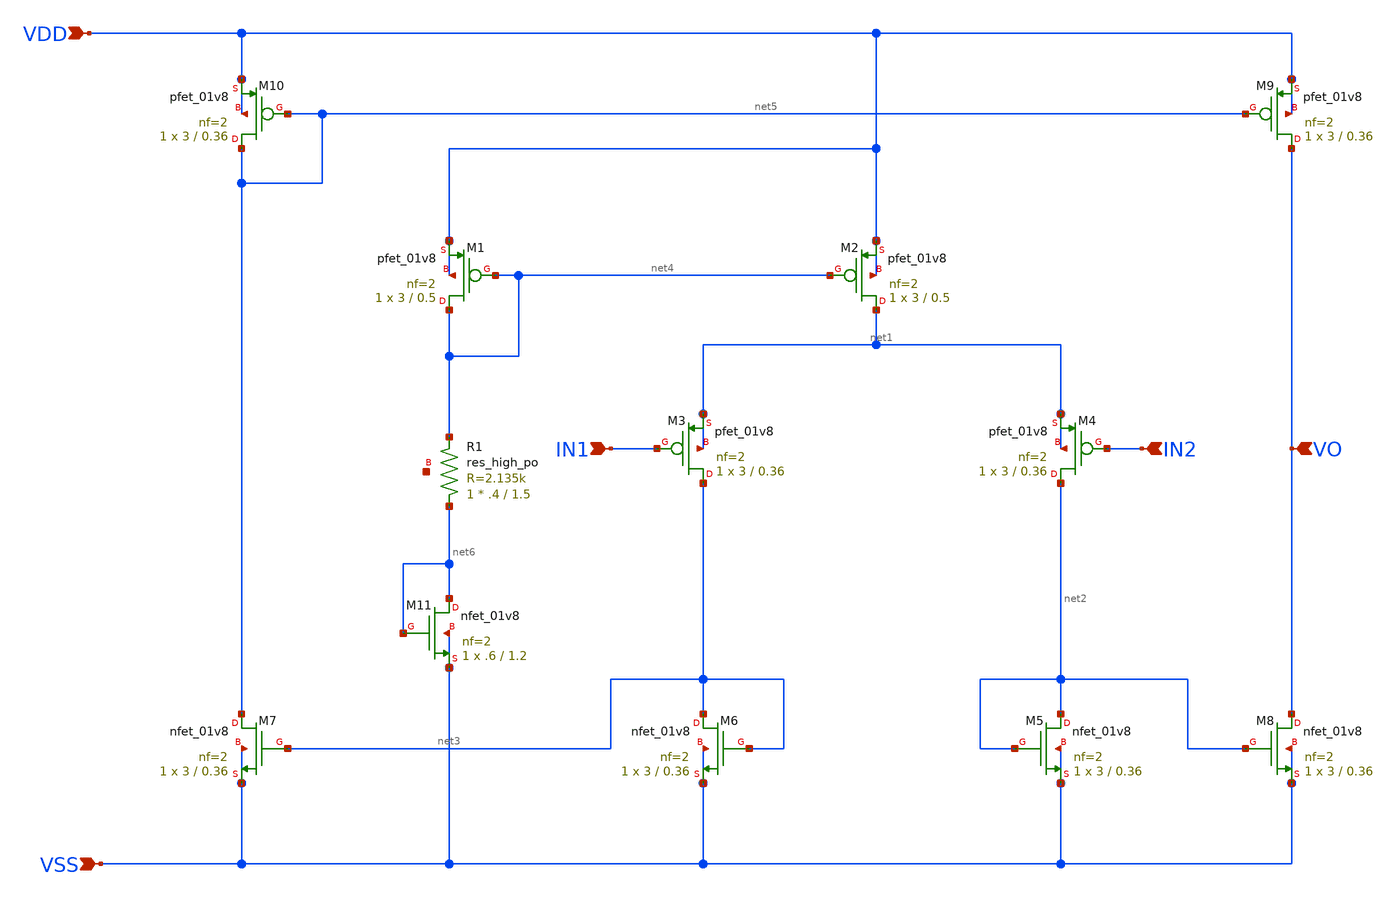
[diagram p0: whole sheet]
** sch_path: design/RPLY_EX0_SKY130NM/OTAP.sch
**.subckt OTAP VDD VSS IN1 IN2 VO
*.ipin VDD
*.ipin VSS
*.ipin IN1
*.ipin IN2
*.ipin VO
XM1 net4 net4 VDD VDD sky130_fd_pr__pfet_01v8 L=0.5 W=3 nf=2 ad='int((nf+1)/2) * W/nf * 0.29' as='int((nf+2)/2) * W/nf * 0.29'
+ pd='2*int((nf+1)/2) * (W/nf + 0.29)' ps='2*int((nf+2)/2) * (W/nf + 0.29)' nrd='0.29 / W' nrs='0.29 / W'
+ sa=0 sb=0 sd=0 mult=1 m=1
XM2 net1 net4 VDD VDD sky130_fd_pr__pfet_01v8 L=0.5 W=3 nf=2 ad='int((nf+1)/2) * W/nf * 0.29' as='int((nf+2)/2) * W/nf * 0.29'
+ pd='2*int((nf+1)/2) * (W/nf + 0.29)' ps='2*int((nf+2)/2) * (W/nf + 0.29)' nrd='0.29 / W' nrs='0.29 / W'
+ sa=0 sb=0 sd=0 mult=1 m=1
XM3 net3 IN1 net1 net1 sky130_fd_pr__pfet_01v8 L=0.36 W=3 nf=2 ad='int((nf+1)/2) * W/nf * 0.29' as='int((nf+2)/2) * W/nf * 0.29'
+ pd='2*int((nf+1)/2) * (W/nf + 0.29)' ps='2*int((nf+2)/2) * (W/nf + 0.29)' nrd='0.29 / W' nrs='0.29 / W'
+ sa=0 sb=0 sd=0 mult=1 m=1
XM4 net2 IN2 net1 net1 sky130_fd_pr__pfet_01v8 L=0.36 W=3 nf=2 ad='int((nf+1)/2) * W/nf * 0.29' as='int((nf+2)/2) * W/nf * 0.29'
+ pd='2*int((nf+1)/2) * (W/nf + 0.29)' ps='2*int((nf+2)/2) * (W/nf + 0.29)' nrd='0.29 / W' nrs='0.29 / W'
+ sa=0 sb=0 sd=0 mult=1 m=1
XM5 net2 net2 VSS VSS sky130_fd_pr__nfet_01v8 L=0.36 W=3 nf=2 ad='int((nf+1)/2) * W/nf * 0.29' as='int((nf+2)/2) * W/nf * 0.29'
+ pd='2*int((nf+1)/2) * (W/nf + 0.29)' ps='2*int((nf+2)/2) * (W/nf + 0.29)' nrd='0.29 / W' nrs='0.29 / W'
+ sa=0 sb=0 sd=0 mult=1 m=1
XM6 net3 net3 VSS VSS sky130_fd_pr__nfet_01v8 L=0.36 W=3 nf=2 ad='int((nf+1)/2) * W/nf * 0.29' as='int((nf+2)/2) * W/nf * 0.29'
+ pd='2*int((nf+1)/2) * (W/nf + 0.29)' ps='2*int((nf+2)/2) * (W/nf + 0.29)' nrd='0.29 / W' nrs='0.29 / W'
+ sa=0 sb=0 sd=0 mult=1 m=1
XM7 net5 net3 VSS VSS sky130_fd_pr__nfet_01v8 L=0.36 W=3 nf=2 ad='int((nf+1)/2) * W/nf * 0.29' as='int((nf+2)/2) * W/nf * 0.29'
+ pd='2*int((nf+1)/2) * (W/nf + 0.29)' ps='2*int((nf+2)/2) * (W/nf + 0.29)' nrd='0.29 / W' nrs='0.29 / W'
+ sa=0 sb=0 sd=0 mult=1 m=1
XM8 VO net2 VSS VSS sky130_fd_pr__nfet_01v8 L=0.36 W=3 nf=2 ad='int((nf+1)/2) * W/nf * 0.29' as='int((nf+2)/2) * W/nf * 0.29'
+ pd='2*int((nf+1)/2) * (W/nf + 0.29)' ps='2*int((nf+2)/2) * (W/nf + 0.29)' nrd='0.29 / W' nrs='0.29 / W'
+ sa=0 sb=0 sd=0 mult=1 m=1
XM9 VO net5 VDD VDD sky130_fd_pr__pfet_01v8 L=0.36 W=3 nf=2 ad='int((nf+1)/2) * W/nf * 0.29' as='int((nf+2)/2) * W/nf * 0.29'
+ pd='2*int((nf+1)/2) * (W/nf + 0.29)' ps='2*int((nf+2)/2) * (W/nf + 0.29)' nrd='0.29 / W' nrs='0.29 / W'
+ sa=0 sb=0 sd=0 mult=1 m=1
XM10 net5 net5 VDD VDD sky130_fd_pr__pfet_01v8 L=0.36 W=3 nf=2 ad='int((nf+1)/2) * W/nf * 0.29' as='int((nf+2)/2) * W/nf * 0.29'
+ pd='2*int((nf+1)/2) * (W/nf + 0.29)' ps='2*int((nf+2)/2) * (W/nf + 0.29)' nrd='0.29 / W' nrs='0.29 / W'
+ sa=0 sb=0 sd=0 mult=1 m=1
XM11 net6 net6 VSS VSS sky130_fd_pr__nfet_01v8 L=1.2 W=.6 nf=2 ad='int((nf+1)/2) * W/nf * 0.29' as='int((nf+2)/2) * W/nf * 0.29'
+ pd='2*int((nf+1)/2) * (W/nf + 0.29)' ps='2*int((nf+2)/2) * (W/nf + 0.29)' nrd='0.29 / W' nrs='0.29 / W'
+ sa=0 sb=0 sd=0 mult=1 m=1
XR1 net6 net4 net7 sky130_fd_pr__res_high_po W=.4 L=1.5 mult=1 m=1
**.ends
.end
